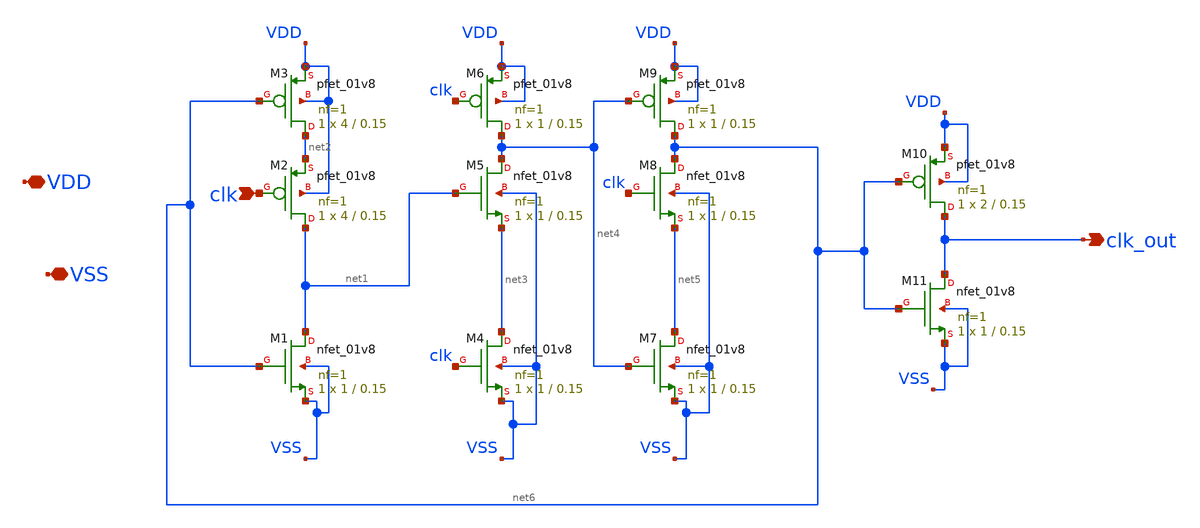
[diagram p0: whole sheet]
** sch_path: xschem/divide_by_two.sch
**.subckt divide_by_two clk_out clk VDD VSS
*.opin clk_out
*.ipin clk
*.iopin VDD
*.iopin VSS
XM1 net1 net6 VSS VSS sky130_fd_pr__nfet_01v8 L=0.15 W=1 nf=1 ad='int((nf+1)/2) * W/nf * 0.29' as='int((nf+2)/2) * W/nf * 0.29'
+ pd='2*int((nf+1)/2) * (W/nf + 0.29)' ps='2*int((nf+2)/2) * (W/nf + 0.29)' nrd='0.29 / W' nrs='0.29 / W'
+ sa=0 sb=0 sd=0 mult=1 m=1
XM2 net1 clk net2 VDD sky130_fd_pr__pfet_01v8 L=0.15 W=4 nf=1 ad='int((nf+1)/2) * W/nf * 0.29' as='int((nf+2)/2) * W/nf * 0.29'
+ pd='2*int((nf+1)/2) * (W/nf + 0.29)' ps='2*int((nf+2)/2) * (W/nf + 0.29)' nrd='0.29 / W' nrs='0.29 / W'
+ sa=0 sb=0 sd=0 mult=1 m=1
XM3 net2 net6 VDD VDD sky130_fd_pr__pfet_01v8 L=0.15 W=4 nf=1 ad='int((nf+1)/2) * W/nf * 0.29' as='int((nf+2)/2) * W/nf * 0.29'
+ pd='2*int((nf+1)/2) * (W/nf + 0.29)' ps='2*int((nf+2)/2) * (W/nf + 0.29)' nrd='0.29 / W' nrs='0.29 / W'
+ sa=0 sb=0 sd=0 mult=1 m=1
XM4 net3 clk VSS VSS sky130_fd_pr__nfet_01v8 L=0.15 W=1 nf=1 ad='int((nf+1)/2) * W/nf * 0.29' as='int((nf+2)/2) * W/nf * 0.29'
+ pd='2*int((nf+1)/2) * (W/nf + 0.29)' ps='2*int((nf+2)/2) * (W/nf + 0.29)' nrd='0.29 / W' nrs='0.29 / W'
+ sa=0 sb=0 sd=0 mult=1 m=1
XM6 net4 clk VDD VDD sky130_fd_pr__pfet_01v8 L=0.15 W=1 nf=1 ad='int((nf+1)/2) * W/nf * 0.29' as='int((nf+2)/2) * W/nf * 0.29'
+ pd='2*int((nf+1)/2) * (W/nf + 0.29)' ps='2*int((nf+2)/2) * (W/nf + 0.29)' nrd='0.29 / W' nrs='0.29 / W'
+ sa=0 sb=0 sd=0 mult=1 m=1
XM7 net5 net4 VSS VSS sky130_fd_pr__nfet_01v8 L=0.15 W=1 nf=1 ad='int((nf+1)/2) * W/nf * 0.29' as='int((nf+2)/2) * W/nf * 0.29'
+ pd='2*int((nf+1)/2) * (W/nf + 0.29)' ps='2*int((nf+2)/2) * (W/nf + 0.29)' nrd='0.29 / W' nrs='0.29 / W'
+ sa=0 sb=0 sd=0 mult=1 m=1
XM9 net6 net4 VDD VDD sky130_fd_pr__pfet_01v8 L=0.15 W=1 nf=1 ad='int((nf+1)/2) * W/nf * 0.29' as='int((nf+2)/2) * W/nf * 0.29'
+ pd='2*int((nf+1)/2) * (W/nf + 0.29)' ps='2*int((nf+2)/2) * (W/nf + 0.29)' nrd='0.29 / W' nrs='0.29 / W'
+ sa=0 sb=0 sd=0 mult=1 m=1
XM5 net4 net1 net3 VSS sky130_fd_pr__nfet_01v8 L=0.15 W=1 nf=1 ad='int((nf+1)/2) * W/nf * 0.29' as='int((nf+2)/2) * W/nf * 0.29'
+ pd='2*int((nf+1)/2) * (W/nf + 0.29)' ps='2*int((nf+2)/2) * (W/nf + 0.29)' nrd='0.29 / W' nrs='0.29 / W'
+ sa=0 sb=0 sd=0 mult=1 m=1
XM8 net6 clk net5 VSS sky130_fd_pr__nfet_01v8 L=0.15 W=1 nf=1 ad='int((nf+1)/2) * W/nf * 0.29' as='int((nf+2)/2) * W/nf * 0.29'
+ pd='2*int((nf+1)/2) * (W/nf + 0.29)' ps='2*int((nf+2)/2) * (W/nf + 0.29)' nrd='0.29 / W' nrs='0.29 / W'
+ sa=0 sb=0 sd=0 mult=1 m=1
XM10 clk_out net6 VDD VDD sky130_fd_pr__pfet_01v8 L=0.15 W=2 nf=1 ad='int((nf+1)/2) * W/nf * 0.29' as='int((nf+2)/2) * W/nf * 0.29'
+ pd='2*int((nf+1)/2) * (W/nf + 0.29)' ps='2*int((nf+2)/2) * (W/nf + 0.29)' nrd='0.29 / W' nrs='0.29 / W'
+ sa=0 sb=0 sd=0 mult=1 m=1
XM11 clk_out net6 VSS VSS sky130_fd_pr__nfet_01v8 L=0.15 W=1 nf=1 ad='int((nf+1)/2) * W/nf * 0.29' as='int((nf+2)/2) * W/nf * 0.29'
+ pd='2*int((nf+1)/2) * (W/nf + 0.29)' ps='2*int((nf+2)/2) * (W/nf + 0.29)' nrd='0.29 / W' nrs='0.29 / W'
+ sa=0 sb=0 sd=0 mult=1 m=1
**.ends
.end
